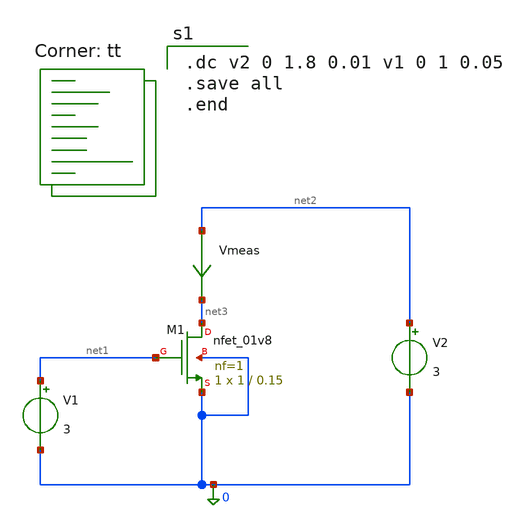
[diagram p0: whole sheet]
** sch_path: Id vs Vgs/Schematic /nmos_dc_sweep.sch
**.subckt nmos_dc_sweep
XM1 net3 net1 0 0 sky130_fd_pr__nfet_01v8 L=0.15 W=1 nf=1 ad='int((1 + 1)/2) * 1 / 1 * 0.29' as='int((1 + 2)/2) * 1 / 1 * 0.29'
+ pd='2*int((1 + 1)/2) * (1 / 1 + 0.29)' ps='2*int((1 + 2)/2) * (1 / 1 + 0.29)' nrd='0.29 / 1 ' nrs='0.29 / 1 '
+ sa=0 sb=0 sd=0 mult=1 m=1
V1 net1 0 3
V2 net2 0 3
Vmeas net2 net3 0
.save i(vmeas)
**** begin user architecture code

.dc v2 0 1.8 0.01 v1 0 1 0.05
.save all
.end


.lib $::SKYWATER_MODELS/sky130.lib.spice tt
**** end user architecture code
**.ends
.end
